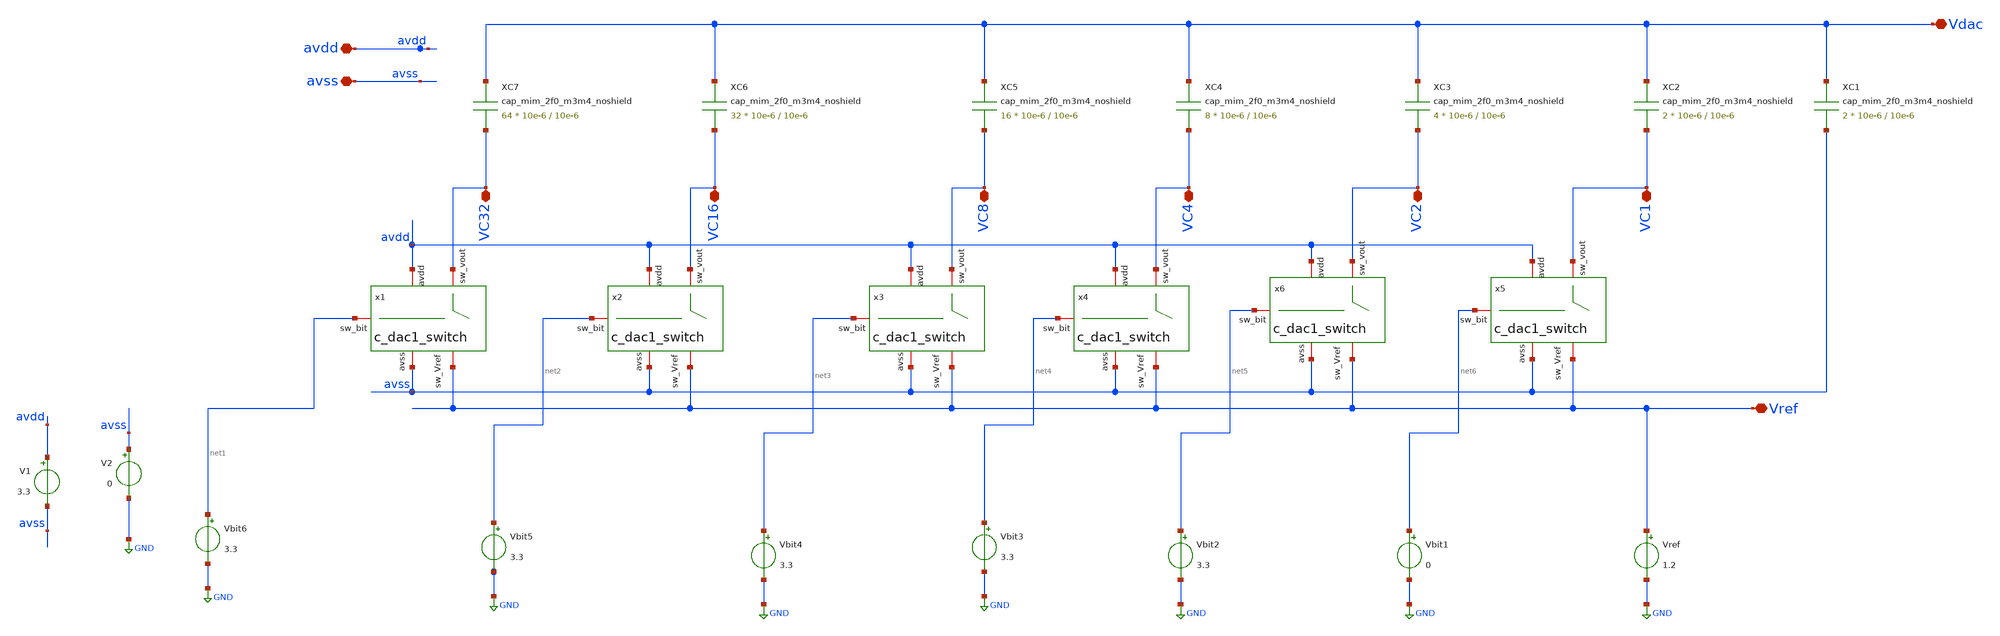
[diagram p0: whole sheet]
** sch_path: designs/libs/WK_Kadam/TB_6bit_CDAC_CO_MK.sch
**.subckt TB_6bit_CDAC_CO_MK Vref VC1 VC2 VC4 VC8 VC16 VC32 Vdac avdd avss
*.iopin Vref
*.iopin VC1
*.iopin VC2
*.iopin VC4
*.iopin VC8
*.iopin VC16
*.iopin VC32
*.iopin Vdac
*.iopin avdd
*.iopin avss
XC3 Vdac VC2 cap_mim_2f0_m3m4_noshield c_width=10e-6 c_length=10e-6 m=4
XC4 Vdac VC4 cap_mim_2f0_m3m4_noshield c_width=10e-6 c_length=10e-6 m=8
XC5 Vdac VC8 cap_mim_2f0_m3m4_noshield c_width=10e-6 c_length=10e-6 m=16
XC6 Vdac VC16 cap_mim_2f0_m3m4_noshield c_width=10e-6 c_length=10e-6 m=32
XC7 Vdac VC32 cap_mim_2f0_m3m4_noshield c_width=10e-6 c_length=10e-6 m=64
x1 avdd avss VC32 net1 Vref c_dac1_switch
x2 avdd avss VC16 net2 Vref c_dac1_switch
x3 avdd avss VC8 net3 Vref c_dac1_switch
x4 avdd avss VC4 net4 Vref c_dac1_switch
x5 avdd avss VC1 net6 Vref c_dac1_switch
x6 avdd avss VC2 net5 Vref c_dac1_switch
V1 avdd avss 3.3
Vbit1 net6 GND 0
Vbit2 net5 GND 3.3
Vbit3 net4 GND 3.3
Vbit4 net3 GND 3.3
Vbit5 net2 GND 3.3
Vbit6 net1 GND 3.3
V2 avss GND 0
Vref Vref GND 1.2
XC1 Vdac avss cap_mim_2f0_m3m4_noshield c_width=10e-6 c_length=10e-6 m=2
XC2 Vdac VC1 cap_mim_2f0_m3m4_noshield c_width=10e-6 c_length=10e-6 m=2
**** begin user architecture code

.include $::180MCU_MODELS/design.ngspice
.lib $::180MCU_MODELS/sm141064.ngspice typical
.lib $::180MCU_MODELS/sm141064.ngspice cap_mim
.lib $::180MCU_MODELS/sm141064.ngspice res_typical
.lib $::180MCU_MODELS/sm141064.ngspice moscap_typical
.lib $::180MCU_MODELS/sm141064.ngspice mimcap_typical
* .lib $::180MCU_MODELS/sm141064.ngspice res_statistical




.control
save all
op
show all
.probe v(Vdac)
alter @Vbit4[DC] = 0
dc Vref 0.8 1.2 0.1
setplot dc1
let Vout = v(Vdac)
plot Vout
tran 10m 30m
setplot tran1
let Vout = v(Vdac)
plot Vout

alter @Vbit6[DC] = 0
dc Vref 0.8 1.2 0.1
setplot dc2
let Vout = v(Vdac)
plot Vout
tran 10m 30m
setplot tran2
let Vout = v(Vdac)
plot Vout
write TB_CDAC_v1.raw
.endc


**** end user architecture code
**.ends

* expanding   symbol:  Wk_Chip_Odyssey/designs/libs/WK_Kadam/c_dac1_switch.sym # of pins=5
** sym_path: designs/libs/WK_Kadam/c_dac1_switch.sym
** sch_path: designs/libs/WK_Kadam/c_dac1_switch.sch
.subckt c_dac1_switch avdd avss sw_vout sw_bit sw_Vref
*.iopin avdd
*.iopin avss
*.iopin sw_bit
*.iopin sw_vout
*.iopin sw_Vref
XM1 sw_vout sw_bit sw_Vref avss nfet_03v3 L=0.28u W=2u nf=1 ad='int((nf+1)/2) * W/nf * 0.18u' as='int((nf+2)/2) * W/nf * 0.18u'
+ pd='2*int((nf+1)/2) * (W/nf + 0.18u)' ps='2*int((nf+2)/2) * (W/nf + 0.18u)' nrd='0.18u / W' nrs='0.18u / W'
+ sa=0 sb=0 sd=0 m=1
XM3 sw_vout net1 avss avss nfet_03v3 L=0.28u W=2u nf=1 ad='int((nf+1)/2) * W/nf * 0.18u' as='int((nf+2)/2) * W/nf * 0.18u'
+ pd='2*int((nf+1)/2) * (W/nf + 0.18u)' ps='2*int((nf+2)/2) * (W/nf + 0.18u)' nrd='0.18u / W' nrs='0.18u / W'
+ sa=0 sb=0 sd=0 m=1
XM4 avss sw_bit sw_vout avdd pfet_03v3 L=0.28u W=2u nf=1 ad='int((nf+1)/2) * W/nf * 0.18u' as='int((nf+2)/2) * W/nf * 0.18u'
+ pd='2*int((nf+1)/2) * (W/nf + 0.18u)' ps='2*int((nf+2)/2) * (W/nf + 0.18u)' nrd='0.18u / W' nrs='0.18u / W'
+ sa=0 sb=0 sd=0 m=1
XM2 sw_Vref net1 sw_vout avdd pfet_03v3 L=0.28u W=2u nf=1 ad='int((nf+1)/2) * W/nf * 0.18u' as='int((nf+2)/2) * W/nf * 0.18u'
+ pd='2*int((nf+1)/2) * (W/nf + 0.18u)' ps='2*int((nf+2)/2) * (W/nf + 0.18u)' nrd='0.18u / W' nrs='0.18u / W'
+ sa=0 sb=0 sd=0 m=1
x1 avdd sw_bit net1 net2 inv_test
.ends


* expanding   symbol:  Wk_Chip_Odyssey/designs/libs/WK_Kadam/inv_test.sym # of pins=4
** sym_path: Wk_Chip_Odyssey/designs/libs/WK_Kadam/inv_test.sym
** sch_path: Wk_Chip_Odyssey/designs/libs/WK_Kadam/inv_test.sch
.subckt inv_test avdd in out avss
*.iopin avdd
*.iopin avss
*.iopin in
*.iopin out
XM3 out in avss avss nfet_03v3 L=0.28u W=1u nf=1 ad='int((nf+1)/2) * W/nf * 0.18u' as='int((nf+2)/2) * W/nf * 0.18u'
+ pd='2*int((nf+1)/2) * (W/nf + 0.18u)' ps='2*int((nf+2)/2) * (W/nf + 0.18u)' nrd='0.18u / W' nrs='0.18u / W'
+ sa=0 sb=0 sd=0 m=1
XM4 out in avdd avdd pfet_03v3 L=0.28u W=2.5u nf=1 ad='int((nf+1)/2) * W/nf * 0.18u' as='int((nf+2)/2) * W/nf * 0.18u'
+ pd='2*int((nf+1)/2) * (W/nf + 0.18u)' ps='2*int((nf+2)/2) * (W/nf + 0.18u)' nrd='0.18u / W' nrs='0.18u / W'
+ sa=0 sb=0 sd=0 m=1
.ends

.GLOBAL GND
.end
